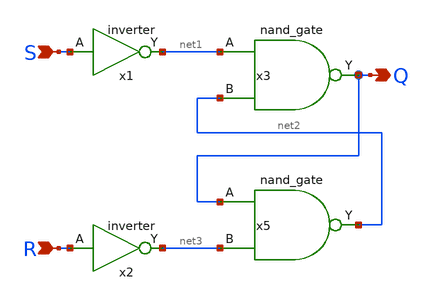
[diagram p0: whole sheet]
** sch_path: 3_real_circuits/sr_latch.sch
**.subckt sr_latch S R Q
*.ipin S
*.ipin R
*.opin Q
x2 R net3 inverter
x3 net1 net2 Q nand_gate
x1 S net1 inverter
x5 Q net3 net2 nand_gate
**.ends

* expanding   symbol:  inverter.sym # of pins=2
** sym_path: 3_real_circuits/inverter.sym
** sch_path: 3_real_circuits/inverter.sch
.subckt inverter A Y
*.opin Y
*.ipin A
XM2 Y A GND GND sg13_hv_nmos w=0.3u l=0.45u ng=1 m=1 mm_ok=1
XM1 Y A VDD VDD sg13_hv_pmos w=0.3u l=0.4u ng=1 m=1 mm_ok=1
.ends


* expanding   symbol:  nand_gate.sym # of pins=3
** sym_path: 3_real_circuits/nand_gate.sym
** sch_path: 3_real_circuits/nand_gate.sch
.subckt nand_gate A B Y
*.ipin A
*.ipin B
*.opin Y
XM1 Y B VDD VDD sg13_hv_pmos w=0.3u l=0.4u ng=1 m=1 mm_ok=1
XM2 Y A VDD VDD sg13_hv_pmos w=0.3u l=0.4u ng=1 m=1 mm_ok=1
XM3 Y A net1 GND sg13_hv_nmos w=0.3u l=0.45u ng=1 m=1 mm_ok=1
XM4 net1 B GND GND sg13_hv_nmos w=0.3u l=0.45u ng=1 m=1 mm_ok=1
.ends

.GLOBAL GND
.GLOBAL VDD
.end
